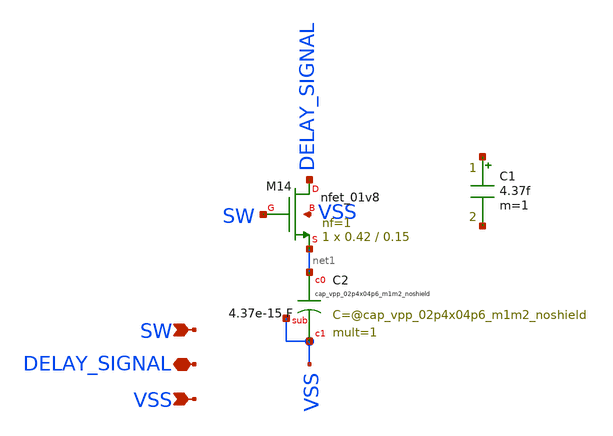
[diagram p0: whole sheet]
** sch_path: hgu/xschem/hgu_sw_cap.sch
**.subckt hgu_sw_cap SW VSS DELAY_SIGNAL
*.ipin SW
*.ipin VSS
*.iopin DELAY_SIGNAL
XM14 DELAY_SIGNAL SW net1 VSS sky130_fd_pr__nfet_01v8 L=0.15 W=0.42 nf=1 ad='int((nf+1)/2) * W/nf * 0.29'
+ as='int((nf+2)/2) * W/nf * 0.29' pd='2*int((nf+1)/2) * (W/nf + 0.29)' ps='2*int((nf+2)/2) * (W/nf + 0.29)'
+ nrd='0.29 / W' nrs='0.29 / W' sa=0 sb=0 sd=0 mult=1 m=1
C1 net2 net3 4.37f m=1
XC2 net1 VSS VSS sky130_fd_pr__cap_vpp_02p4x04p6_m1m2_noshield mult=1 m=1
**.ends
.end
